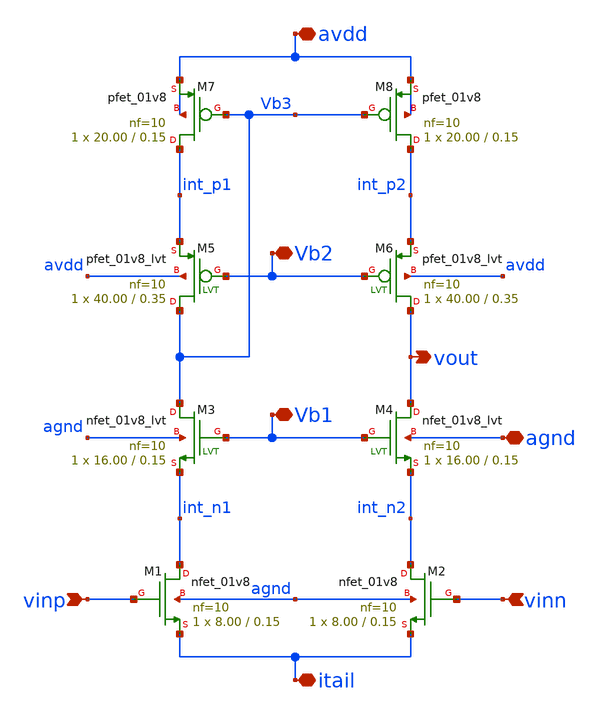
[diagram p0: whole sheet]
** sch_path: AMP/Hard_Cascode.sch
**.subckt Hard_Cascode avdd vinp vout agnd vinn Vb2 Vb1 itail
*.iopin avdd
*.ipin vinp
*.opin vout
*.iopin agnd
*.ipin vinn
*.iopin Vb2
*.iopin Vb1
*.iopin itail
XM1 int_n1 vinp itail agnd sky130_fd_pr__nfet_01v8 L=0.15 W=8.00 nf=10 ad='int((nf+1)/2) * W/nf * 0.29'
+ as='int((nf+2)/2) * W/nf * 0.29' pd='2*int((nf+1)/2) * (W/nf + 0.29)' ps='2*int((nf+2)/2) * (W/nf + 0.29)'
+ nrd='0.29 / W' nrs='0.29 / W' sa=0 sb=0 sd=0 mult=1 m=1
XM2 int_n2 vinn itail agnd sky130_fd_pr__nfet_01v8 L=0.15 W=8.00 nf=10 ad='int((nf+1)/2) * W/nf * 0.29'
+ as='int((nf+2)/2) * W/nf * 0.29' pd='2*int((nf+1)/2) * (W/nf + 0.29)' ps='2*int((nf+2)/2) * (W/nf + 0.29)'
+ nrd='0.29 / W' nrs='0.29 / W' sa=0 sb=0 sd=0 mult=1 m=1
XM7 int_p1 Vb3 avdd avdd sky130_fd_pr__pfet_01v8 L=0.15 W=20.00 nf=10 ad='int((nf+1)/2) * W/nf * 0.29'
+ as='int((nf+2)/2) * W/nf * 0.29' pd='2*int((nf+1)/2) * (W/nf + 0.29)' ps='2*int((nf+2)/2) * (W/nf + 0.29)'
+ nrd='0.29 / W' nrs='0.29 / W' sa=0 sb=0 sd=0 mult=1 m=1
XM8 int_p2 Vb3 avdd avdd sky130_fd_pr__pfet_01v8 L=0.15 W=20.00 nf=10 ad='int((nf+1)/2) * W/nf * 0.29'
+ as='int((nf+2)/2) * W/nf * 0.29' pd='2*int((nf+1)/2) * (W/nf + 0.29)' ps='2*int((nf+2)/2) * (W/nf + 0.29)'
+ nrd='0.29 / W' nrs='0.29 / W' sa=0 sb=0 sd=0 mult=1 m=1
XM3 Vb3 Vb1 int_n1 agnd sky130_fd_pr__nfet_01v8_lvt L=0.15 W=16.00 nf=10 ad='int((nf+1)/2) * W/nf * 0.29'
+ as='int((nf+2)/2) * W/nf * 0.29' pd='2*int((nf+1)/2) * (W/nf + 0.29)' ps='2*int((nf+2)/2) * (W/nf + 0.29)'
+ nrd='0.29 / W' nrs='0.29 / W' sa=0 sb=0 sd=0 mult=1 m=1
XM4 vout Vb1 int_n2 agnd sky130_fd_pr__nfet_01v8_lvt L=0.15 W=16.00 nf=10 ad='int((nf+1)/2) * W/nf * 0.29'
+ as='int((nf+2)/2) * W/nf * 0.29' pd='2*int((nf+1)/2) * (W/nf + 0.29)' ps='2*int((nf+2)/2) * (W/nf + 0.29)'
+ nrd='0.29 / W' nrs='0.29 / W' sa=0 sb=0 sd=0 mult=1 m=1
XM5 Vb3 Vb2 int_p1 avdd sky130_fd_pr__pfet_01v8_lvt L=0.35 W=40.00 nf=10 ad='int((nf+1)/2) * W/nf * 0.29'
+ as='int((nf+2)/2) * W/nf * 0.29' pd='2*int((nf+1)/2) * (W/nf + 0.29)' ps='2*int((nf+2)/2) * (W/nf + 0.29)'
+ nrd='0.29 / W' nrs='0.29 / W' sa=0 sb=0 sd=0 mult=1 m=1
XM6 vout Vb2 int_p2 avdd sky130_fd_pr__pfet_01v8_lvt L=0.35 W=40.00 nf=10 ad='int((nf+1)/2) * W/nf * 0.29'
+ as='int((nf+2)/2) * W/nf * 0.29' pd='2*int((nf+1)/2) * (W/nf + 0.29)' ps='2*int((nf+2)/2) * (W/nf + 0.29)'
+ nrd='0.29 / W' nrs='0.29 / W' sa=0 sb=0 sd=0 mult=1 m=1
**** begin user architecture code
type=primative
**** end user architecture code
**.ends
.end
